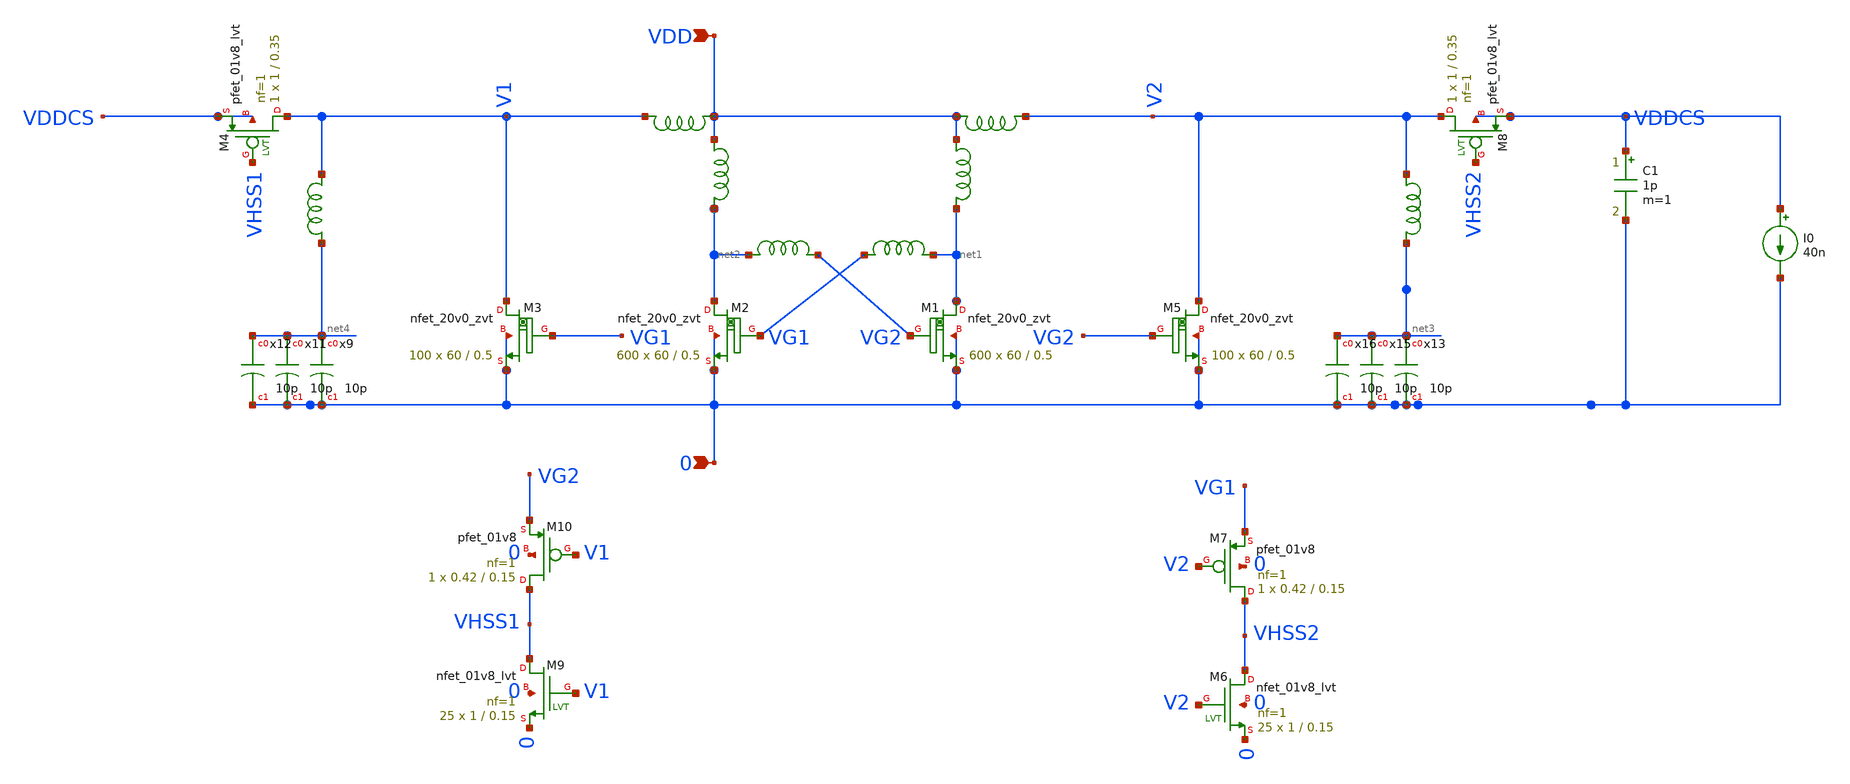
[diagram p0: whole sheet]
** sch_path: design/LELO_SVOD_SKY130A/LELO_EXSC.sch
**.subckt LELO_EXSC 0 VDD
*.ipin 0
*.ipin VDD
x3 VDD net1 1812PS-102_imp
x4 VDD net2 1812PS-102_imp
XM1 net1 VG2 0 0 sky130_fd_pr__nfet_20v0_zvt W=60 L=0.5 m=600
XM2 net2 VG1 0 0 sky130_fd_pr__nfet_20v0_zvt W=60 L=0.5 m=600
x1 net2 VG2 1812PS-104_imp
x2 VG1 net1 1812PS-104_imp
C1 VDDCS 0 1p m=1
XM3 V1 VG1 0 0 sky130_fd_pr__nfet_20v0_zvt W=60 L=0.5 m=100
XM5 V2 VG2 0 0 sky130_fd_pr__nfet_20v0_zvt W=60 L=0.5 m=100
XM7 VHSS2 V2 VG1 0 sky130_fd_pr__pfet_01v8 L=0.15 W=0.42 nf=1 ad='int((1 + 1)/2) * 0.42 / 1 * 0.29' as='int((1 + 2)/2) * 0.42 / 1 * 0.29'
+ pd='2*int((1 + 1)/2) * (0.42 / 1 + 0.29)' ps='2*int((1 + 2)/2) * (0.42 / 1 + 0.29)' nrd='0.29 / 0.42 '
+ nrs='0.29 / 0.42 ' sa=0 sb=0 sd=0 mult=1 m=1
I0 VDDCS 0 40n
x7 V2 net3 1812PS-334_imp
x6 V2 VDD 1812PS-334_imp
x5 VDD V1 1812PS-334_imp
x8 V1 net4 1812PS-334_imp
XM10 VHSS1 V1 VG2 0 sky130_fd_pr__pfet_01v8 L=0.15 W=0.42 nf=1 ad='int((1 + 1)/2) * 0.42 / 1 * 0.29'
+ as='int((1 + 2)/2) * 0.42 / 1 * 0.29' pd='2*int((1 + 1)/2) * (0.42 / 1 + 0.29)' ps='2*int((1 + 2)/2) * (0.42 / 1 + 0.29)'
+ nrd='0.29 / 0.42 ' nrs='0.29 / 0.42 ' sa=0 sb=0 sd=0 mult=1 m=1
XM4 V1 VHSS1 VDDCS VDDCS sky130_fd_pr__pfet_01v8_lvt L=0.35 W=1 nf=1 ad='int((1 + 1)/2) * 1 / 1 * 0.29'
+ as='int((1 + 2)/2) * 1 / 1 * 0.29' pd='2*int((1 + 1)/2) * (1 / 1 + 0.29)' ps='2*int((1 + 2)/2) * (1 / 1 + 0.29)'
+ nrd='0.29 / 1 ' nrs='0.29 / 1 ' sa=0 sb=0 sd=0 mult=1 m=1
XM8 V2 VHSS2 VDDCS VDDCS sky130_fd_pr__pfet_01v8_lvt L=0.35 W=1 nf=1 ad='int((1 + 1)/2) * 1 / 1 * 0.29'
+ as='int((1 + 2)/2) * 1 / 1 * 0.29' pd='2*int((1 + 1)/2) * (1 / 1 + 0.29)' ps='2*int((1 + 2)/2) * (1 / 1 + 0.29)'
+ nrd='0.29 / 1 ' nrs='0.29 / 1 ' sa=0 sb=0 sd=0 mult=1 m=1
x9 net4 0 DK11XEA100K86RBH01_DC0V_20degC
x11 net4 0 DK11XEA100K86RBH01_DC0V_20degC
x12 net4 0 DK11XEA100K86RBH01_DC0V_20degC
x13 net3 0 DK11XEA100K86RBH01_DC0V_20degC
x15 net3 0 DK11XEA100K86RBH01_DC0V_20degC
x16 net3 0 DK11XEA100K86RBH01_DC0V_20degC
XM6 VHSS2 V2 0 0 sky130_fd_pr__nfet_01v8_lvt L=0.15 W=1 nf=1 ad='int((1 + 1)/2) * 1 / 1 * 0.29' as='int((1 + 2)/2) * 1 / 1 * 0.29'
+ pd='2*int((1 + 1)/2) * (1 / 1 + 0.29)' ps='2*int((1 + 2)/2) * (1 / 1 + 0.29)' nrd='0.29 / 1 ' nrs='0.29 / 1 '
+ sa=0 sb=0 sd=0 mult=25 m=25
XM9 VHSS1 V1 0 0 sky130_fd_pr__nfet_01v8_lvt L=0.15 W=1 nf=1 ad='int((1 + 1)/2) * 1 / 1 * 0.29' as='int((1 + 2)/2) * 1 / 1 * 0.29'
+ pd='2*int((1 + 1)/2) * (1 / 1 + 0.29)' ps='2*int((1 + 2)/2) * (1 / 1 + 0.29)' nrd='0.29 / 1 ' nrs='0.29 / 1 '
+ sa=0 sb=0 sd=0 mult=25 m=25
**.ends

* expanding   symbol:  LELO_SVOD_SKY130A/1812PS-102_imp.sym # of pins=2
** sym_path: design/LELO_SVOD_SKY130A/1812PS-102_imp.sym

.subckt 1812PS-102_imp port1 port2
X1 port1 port2 Model1D R1=60 R2=0.054 C= 0.15p K1=0.000001 K2=0.064 K3= 1u K4=1E-06 K5=0.000001 L=0
+ Is=0 a=0 L_Z0=0 L_EL=0 L_F0=0E6 PkZ=1282.46492
.ends 1812PS-102_imp

* expanding   symbol:  LELO_SVOD_SKY130A/1812PS-104_imp.sym # of pins=2
** sym_path: design/LELO_SVOD_SKY130A/1812PS-104_imp.sym

.subckt 1812PS-104_imp port1 port2
X1 port1 port2 Model1D R1=40 R2=1.3 C= 1.6p K1=0.000001 K2=13.98 K3= 100u K4=0.000001 K5=0.000001
+ L=0 Is=0 a=0 L_Z0=0 L_EL=0 L_F0=0E6 PkZ=48065.0165
.ends 1812PS-104_imp

* expanding   symbol:  LELO_SVOD_SKY130A/1812PS-334_imp.sym # of pins=2
** sym_path: design/LELO_SVOD_SKY130A/1812PS-334_imp.sym

.subckt 1812PS-334_imp port1 port2
X1 port1 port2 Model1D R1=75 R2=4.9 C= 2.43p K1=1E-06 K2=57.9 K3= 330u K4=0.000001 K5=0.000001 L=0
+ Is=0 a=0 L_Z0=0 L_EL=0 L_F0=0E6 PkZ=127597.141
.ends 1812PS-334_imp


* expanding   symbol:  LELO_SVOD_SKY130A/DK11XEA100K86RBH01_DC0V_20degC.sym # of pins=2
** sym_path: design/LELO_SVOD_SKY130A/DK11XEA100K86RBH01_DC0V_20degC.sym

.SUBCKT DK11XEA100K86RBH01_DC0V_20degC port1 port2
C1 port1 11 1.02e-11
L2 11 12 1.22e-9
R3 12 13 2.71e-1
C4 13 14 1.51e-9
R4 13 14 1.06e+3
C5 14 15 2.34e-9
R5 14 15 20.0
C6 15 16 2.30e-8
R6 15 16 9.28e-2
L7 16 17 1.69e-10
R7 16 17 4.28e-1
C8 17 18 1.34e-9
L8 17 18 3.17e-10
R8 17 18 6.85e-1
C9 18 19 1.27e-11
L9 18 19 2.18e-10
R9 18 19 26.0
C10 19 port2 1.06e-12
L10 19 port2 1.71e-9
R10 19 port2 889
R100 port1 11 6.00e+9
.ENDS DK11XEA100K86RBH01_DC0V_20degC

.end
